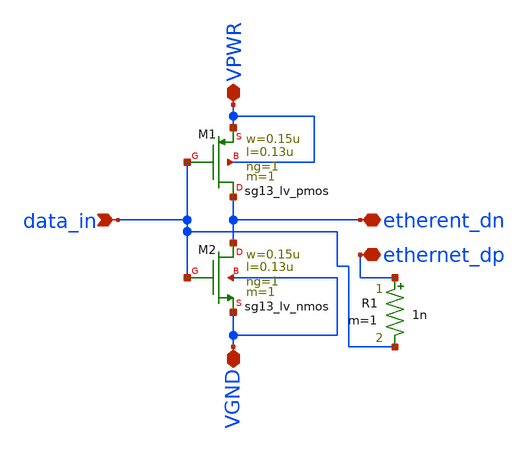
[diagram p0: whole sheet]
** sch_path: xschem/ethernet_analog.sch
**.subckt ethernet_analog data_in etherent_dn VGND VPWR ethernet_dp
*.ipin data_in
*.iopin etherent_dn
*.iopin VGND
*.iopin VPWR
*.iopin ethernet_dp
XM2 etherent_dn data_in VGND VGND sg13_lv_nmos w=0.15u l=0.13u ng=1 m=1 mm_ok=1
XM1 etherent_dn data_in VPWR VPWR sg13_lv_pmos w=0.15u l=0.13u ng=1 m=1 mm_ok=1
R1 ethernet_dp data_in 1n m=1
**.ends
.end
